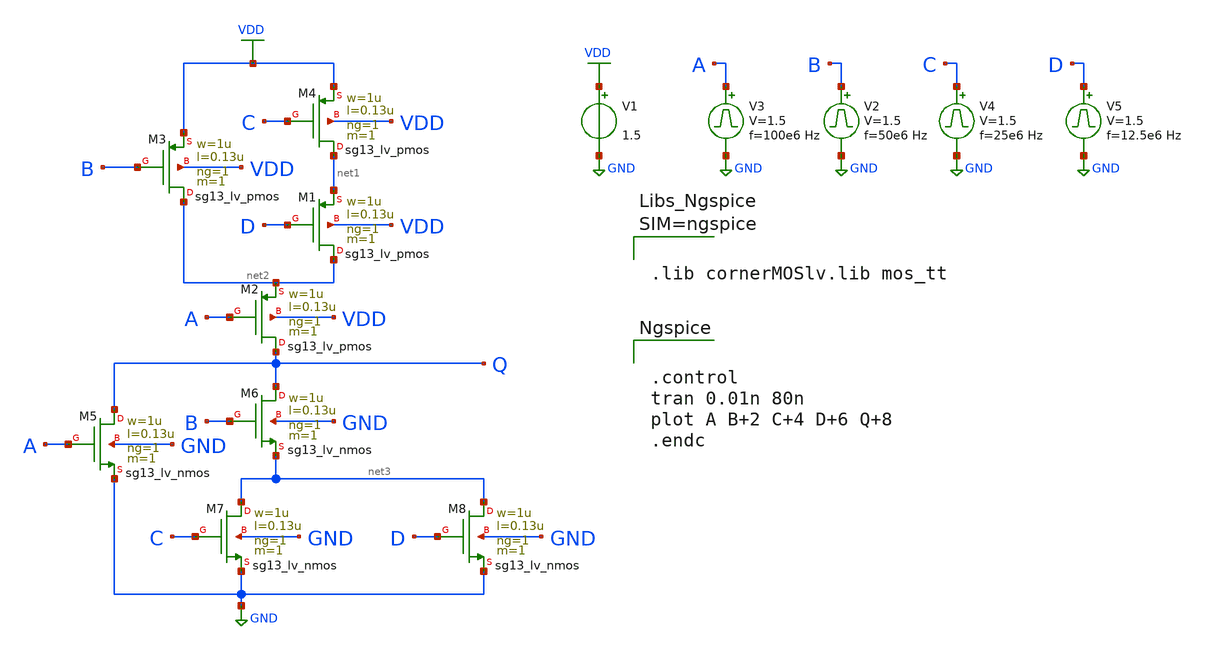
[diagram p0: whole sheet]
** sch_path: Modulo_Digital/Lab1/cmos_funct1.sch
**.subckt cmos_funct1
V1 VDD GND 1.5
V3 A GND pulse 0 1.5 '0.495/ 100e6 ' '0.01/100e6 ' '0.01/100e6 ' '0.49/100e6 ' '1/100e6 '
V2 B GND pulse 0 1.5 '0.495/ 50e6 ' '0.01/50e6 ' '0.01/50e6 ' '0.49/50e6 ' '1/50e6 '
V4 C GND pulse 0 1.5 '0.495/ 25e6 ' '0.01/25e6 ' '0.01/25e6 ' '0.49/25e6 ' '1/25e6 '
V5 D GND pulse 0 1.5 '0.495/ 12.5e6 ' '0.01/12.5e6 ' '0.01/12.5e6 ' '0.49/12.5e6 ' '1/12.5e6 '
XM1 net2 D net1 VDD sg13_lv_pmos w=1u l=0.13u ng=1 m=1 mm_ok=1
XM2 Q A net2 VDD sg13_lv_pmos w=1u l=0.13u ng=1 m=1 mm_ok=1
XM3 net2 B VDD VDD sg13_lv_pmos w=1u l=0.13u ng=1 m=1 mm_ok=1
XM4 net1 C VDD VDD sg13_lv_pmos w=1u l=0.13u ng=1 m=1 mm_ok=1
XM5 Q A GND GND sg13_lv_nmos w=1u l=0.13u ng=1 m=1 mm_ok=1
XM6 Q B net3 GND sg13_lv_nmos w=1u l=0.13u ng=1 m=1 mm_ok=1
XM7 net3 C GND GND sg13_lv_nmos w=1u l=0.13u ng=1 m=1 mm_ok=1
XM8 net3 D GND GND sg13_lv_nmos w=1u l=0.13u ng=1 m=1 mm_ok=1
**** begin user architecture code


.control
tran 0.01n 80n
plot A B+2 C+4 D+6 Q+8
.endc




.lib cornerMOSlv.lib mos_tt



**** end user architecture code
**.ends
.GLOBAL GND
.GLOBAL VDD
.end
